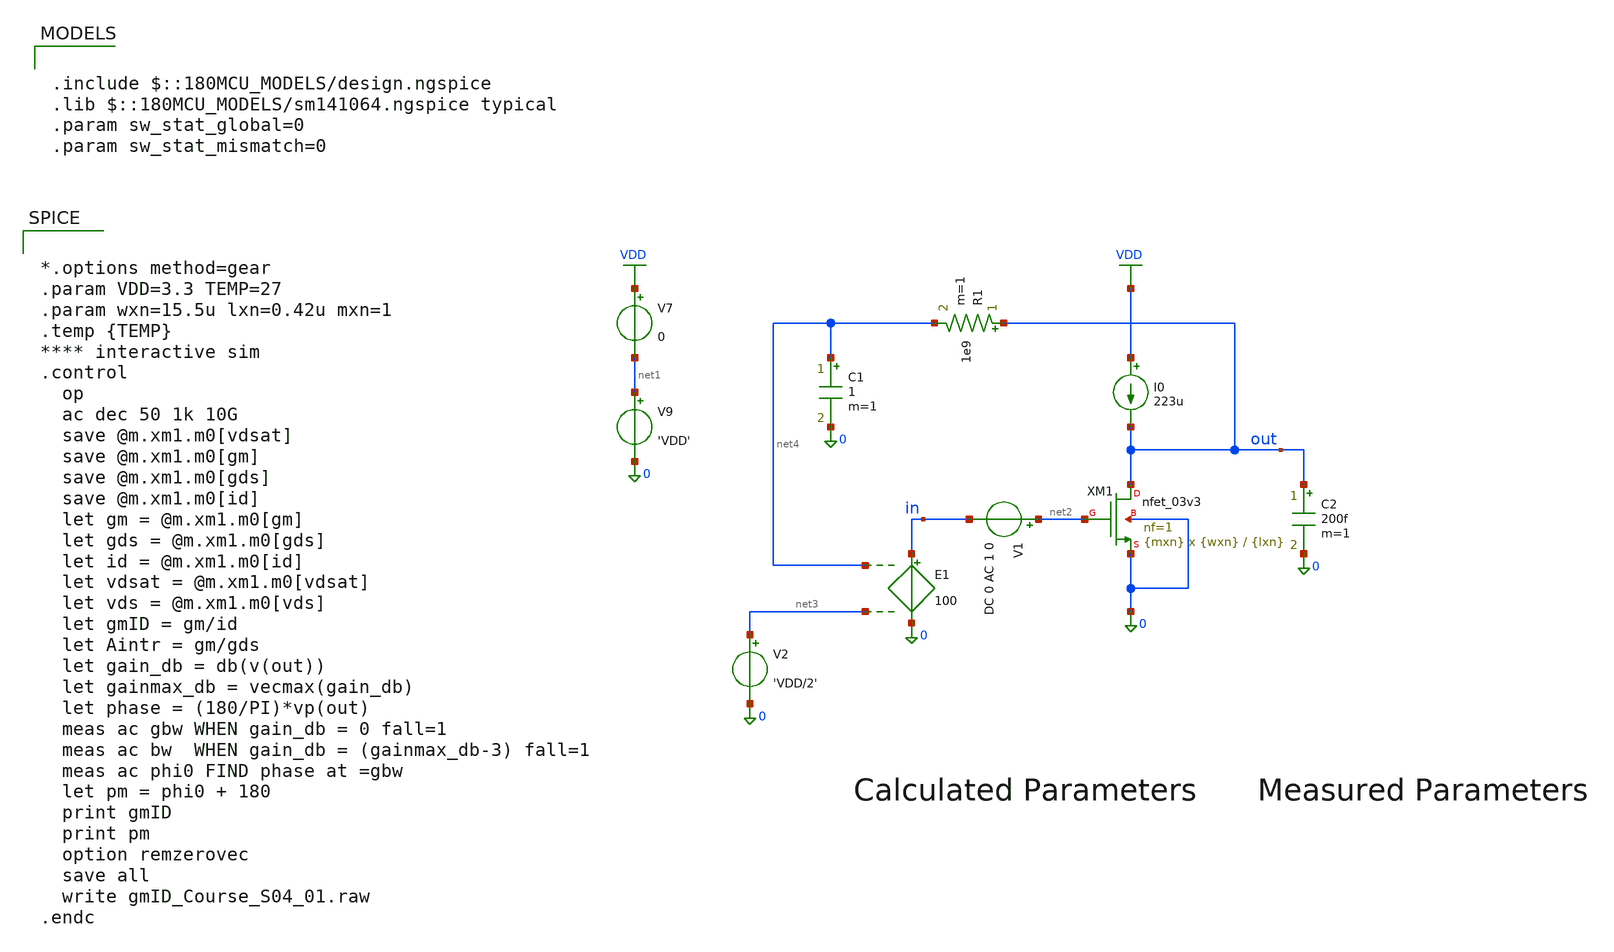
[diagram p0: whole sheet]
** sch_path: Xschem/gf180mcuD/gmID_Designs/gmID_Course_S04_01.sch
**.subckt gmID_Course_S04_01
XM1 out net2 0 0 nfet_03v3 L={lxn} W={wxn} nf=1 ad='int((nf+1)/2) * W/nf * 0.18u' as='int((nf+2)/2) * W/nf * 0.18u'
+ pd='2*int((nf+1)/2) * (W/nf + 0.18u)' ps='2*int((nf+2)/2) * (W/nf + 0.18u)' nrd='0.18u / W' nrs='0.18u / W'
+ sa=0 sb=0 sd=0 m={mxn}
I0 VDD out 223u
E1 in 0 net4 net3 100
R1 out net4 1e9 m=1
C1 net4 0 1 m=1
V1 net2 in DC 0 AC 1 0
V9 net1 0 'VDD'
V7 VDD net1 0
C2 out 0 200f m=1
V2 net3 0 'VDD/2'
**** begin user architecture code

.include $::180MCU_MODELS/design.ngspice
.lib $::180MCU_MODELS/sm141064.ngspice typical
.param sw_stat_global=0
.param sw_stat_mismatch=0



*.options method=gear
.param VDD=3.3 TEMP=27
.param wxn=15.5u lxn=0.42u mxn=1
.temp {TEMP}
**** interactive sim
.control
  op
  ac dec 50 1k 10G
  save @m.xm1.m0[vdsat]
  save @m.xm1.m0[gm]
  save @m.xm1.m0[gds]
  save @m.xm1.m0[id]
  let gm = @m.xm1.m0[gm]
  let gds = @m.xm1.m0[gds]
  let id = @m.xm1.m0[id]
  let vdsat = @m.xm1.m0[vdsat]
  let vds = @m.xm1.m0[vds]
  let gmID = gm/id
  let Aintr = gm/gds
  let gain_db = db(v(out))
  let gainmax_db = vecmax(gain_db)
  let phase = (180/PI)*vp(out)
  meas ac gbw WHEN gain_db = 0 fall=1
  meas ac bw  WHEN gain_db = (gainmax_db-3) fall=1
  meas ac phi0 FIND phase at =gbw
  let pm = phi0 + 180
  print gmID
  print pm
  option remzerovec
  save all
  write gmID_Course_S04_01.raw
.endc


**** end user architecture code
**.ends
.GLOBAL VDD
.end
